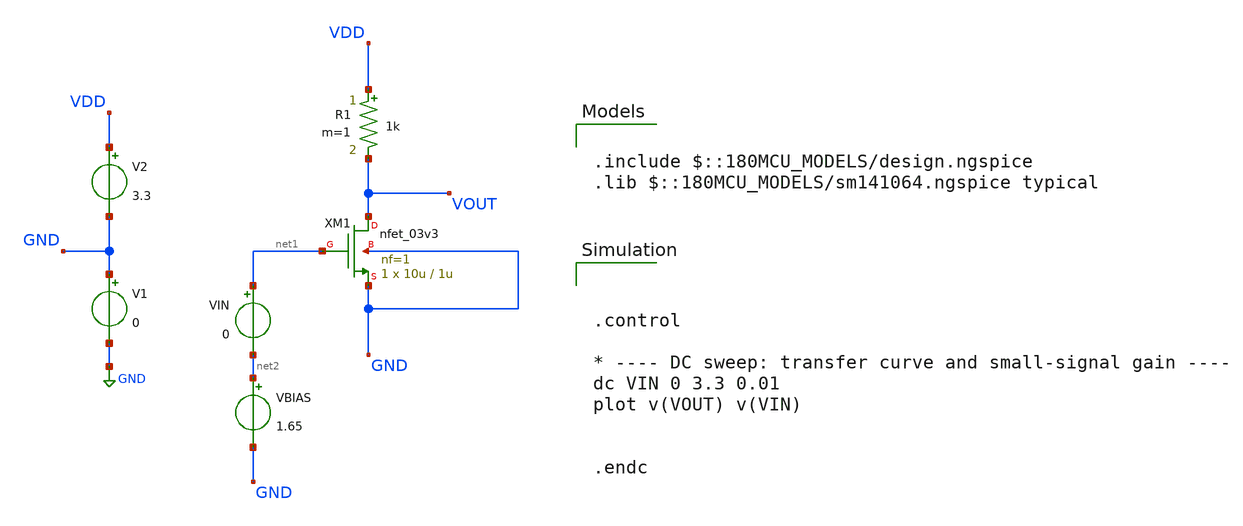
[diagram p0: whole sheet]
** sch_path: designs/libs/session_1/cs_res_load.sch
**.subckt cs_res_load
XM1 VOUT net1 GND GND nfet_03v3 L=1u W=10u nf=1 ad='int((nf+1)/2) * W/nf * 0.18u' as='int((nf+2)/2) * W/nf * 0.18u'
+ pd='2*int((nf+1)/2) * (W/nf + 0.18u)' ps='2*int((nf+2)/2) * (W/nf + 0.18u)' nrd='0.18u / W' nrs='0.18u / W'
+ sa=0 sb=0 sd=0 m=1
R1 VDD VOUT 1k m=1
V1 GND GND 0
V2 VDD GND 3.3
VBIAS net2 GND 1.65
VIN net1 net2 0
**** begin user architecture code



.control

* ---- DC sweep: transfer curve and small-signal gain ----
dc VIN 0 3.3 0.01
plot v(VOUT) v(VIN)


.endc



.include $::180MCU_MODELS/design.ngspice
.lib $::180MCU_MODELS/sm141064.ngspice typical

**** end user architecture code
**.ends
.GLOBAL GND
.end
